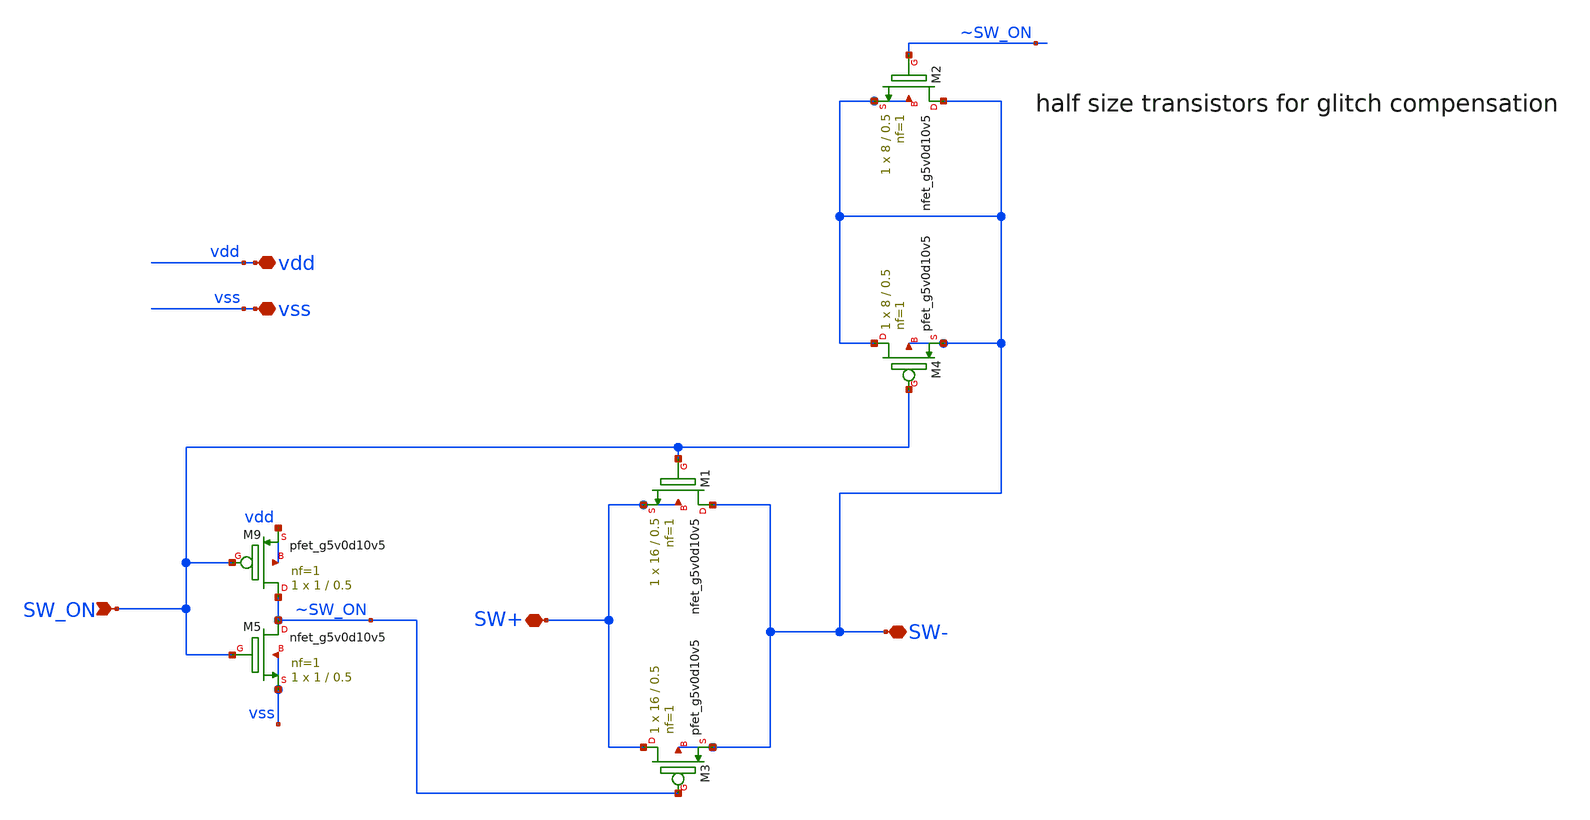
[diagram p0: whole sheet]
** sch_path: xschem/analog_switch.sch
**.subckt analog_switch vdd vss SW_ON SW+ SW-
*.iopin vdd
*.iopin vss
*.ipin SW_ON
*.iopin SW+
*.iopin SW-
XM5 ~SW_ON SW_ON vss vss sky130_fd_pr__nfet_g5v0d10v5 L=0.5 W=1 nf=1 ad='int((1 + 1)/2) * 1 / 1 * 0.29'
+ as='int((1 + 2)/2) * 1 / 1 * 0.29' pd='2*int((1 + 1)/2) * (1 / 1 + 0.29)' ps='2*int((1 + 2)/2) * (1 / 1 + 0.29)'
+ nrd='0.29 / 1 ' nrs='0.29 / 1 ' sa=0 sb=0 sd=0 mult=1 m=1
XM9 ~SW_ON SW_ON vdd vdd sky130_fd_pr__pfet_g5v0d10v5 L=0.5 W=1 nf=1 ad='int((1 + 1)/2) * 1 / 1 * 0.29'
+ as='int((1 + 2)/2) * 1 / 1 * 0.29' pd='2*int((1 + 1)/2) * (1 / 1 + 0.29)' ps='2*int((1 + 2)/2) * (1 / 1 + 0.29)'
+ nrd='0.29 / 1 ' nrs='0.29 / 1 ' sa=0 sb=0 sd=0 mult=1 m=1
XM1 SW- SW_ON SW+ SW+ sky130_fd_pr__nfet_g5v0d10v5 L=0.5 W=16 nf=1 ad='int((1 + 1)/2) * 16 / 1 * 0.29'
+ as='int((1 + 2)/2) * 16 / 1 * 0.29' pd='2*int((1 + 1)/2) * (16 / 1 + 0.29)' ps='2*int((1 + 2)/2) * (16 / 1 + 0.29)'
+ nrd='0.29 / 16 ' nrs='0.29 / 16 ' sa=0 sb=0 sd=0 mult=1 m=1
XM3 SW+ ~SW_ON SW- SW- sky130_fd_pr__pfet_g5v0d10v5 L=0.5 W=16 nf=1 ad='int((1 + 1)/2) * 16 / 1 * 0.29'
+ as='int((1 + 2)/2) * 16 / 1 * 0.29' pd='2*int((1 + 1)/2) * (16 / 1 + 0.29)' ps='2*int((1 + 2)/2) * (16 / 1 + 0.29)'
+ nrd='0.29 / 16 ' nrs='0.29 / 16 ' sa=0 sb=0 sd=0 mult=1 m=1
XM2 SW- ~SW_ON SW- SW- sky130_fd_pr__nfet_g5v0d10v5 L=0.5 W=8 nf=1 ad='int((1 + 1)/2) * 8 / 1 * 0.29'
+ as='int((1 + 2)/2) * 8 / 1 * 0.29' pd='2*int((1 + 1)/2) * (8 / 1 + 0.29)' ps='2*int((1 + 2)/2) * (8 / 1 + 0.29)'
+ nrd='0.29 / 8 ' nrs='0.29 / 8 ' sa=0 sb=0 sd=0 mult=1 m=1
XM4 SW- SW_ON SW- SW- sky130_fd_pr__pfet_g5v0d10v5 L=0.5 W=8 nf=1 ad='int((1 + 1)/2) * 8 / 1 * 0.29'
+ as='int((1 + 2)/2) * 8 / 1 * 0.29' pd='2*int((1 + 1)/2) * (8 / 1 + 0.29)' ps='2*int((1 + 2)/2) * (8 / 1 + 0.29)'
+ nrd='0.29 / 8 ' nrs='0.29 / 8 ' sa=0 sb=0 sd=0 mult=1 m=1
**** begin user architecture code
Target 1mA switching current
**** end user architecture code
**.ends
.end
